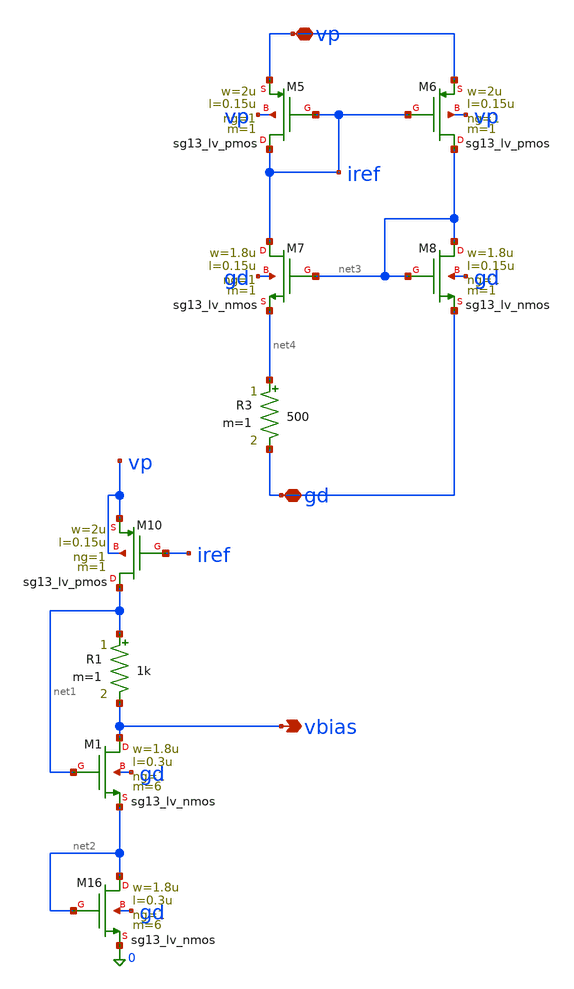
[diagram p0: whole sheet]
** sch_path: schematics/charge_pump/vbias_n.sch
**.subckt vbias_n vp gd vbias
*.iopin vp
*.iopin gd
*.opin vbias
XM16 net2 net2 0 gd sg13_lv_nmos w=1.8u l=0.3u ng=1 m=6 mm_ok=1
XM1 vbias net1 net2 gd sg13_lv_nmos w=1.8u l=0.3u ng=1 m=6 mm_ok=1
R1 net1 vbias 1k m=1
XM5 iref iref vp vp sg13_lv_pmos w=2u l=0.15u ng=1 m=1 mm_ok=1
XM6 net3 iref vp vp sg13_lv_pmos w=2u l=0.15u ng=1 m=1 mm_ok=1
XM7 iref net3 net4 gd sg13_lv_nmos w=1.8u l=0.15u ng=1 m=1 mm_ok=1
XM8 net3 net3 gd gd sg13_lv_nmos w=1.8u l=0.15u ng=1 m=1 mm_ok=1
R3 net4 gd 500 m=1
XM10 net1 iref vp vp sg13_lv_pmos w=2u l=0.15u ng=1 m=1 mm_ok=1
**.ends
.end
